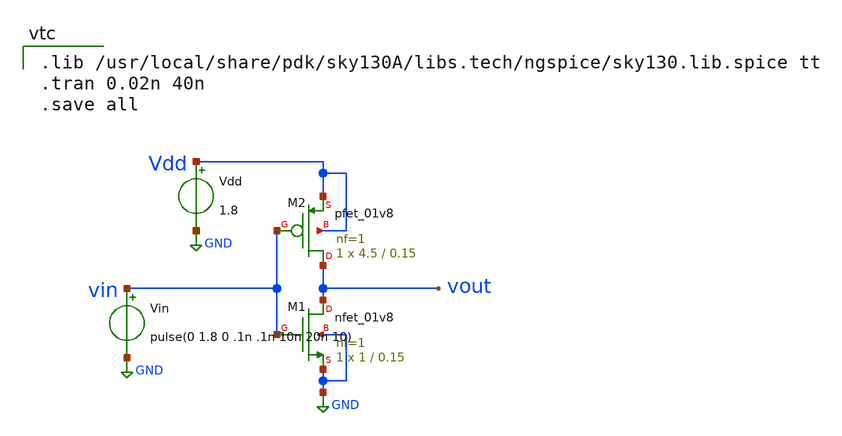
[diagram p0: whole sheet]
** sch_path: vtc_inv.sch
**.subckt vtc_inv
XM1 vout vin GND GND sky130_fd_pr__nfet_01v8 L=0.15 W=1 nf=1 ad='int((nf+1)/2) * W/nf * 0.29' as='int((nf+2)/2) * W/nf * 0.29'
+ pd='2*int((nf+1)/2) * (W/nf + 0.29)' ps='2*int((nf+2)/2) * (W/nf + 0.29)' nrd='0.29 / W' nrs='0.29 / W'
+ sa=0 sb=0 sd=0 mult=1 m=1
XM2 vout vin Vdd Vdd sky130_fd_pr__pfet_01v8 L=0.15 W=4.5 nf=1 ad='int((nf+1)/2) * W/nf * 0.29' as='int((nf+2)/2) * W/nf * 0.29'
+ pd='2*int((nf+1)/2) * (W/nf + 0.29)' ps='2*int((nf+2)/2) * (W/nf + 0.29)' nrd='0.29 / W' nrs='0.29 / W'
+ sa=0 sb=0 sd=0 mult=1 m=1
Vin vin GND pulse(0 1.8 0 .1n .1n 10n 20n 10)
Vdd Vdd GND 1.8
**** begin user architecture code

.lib /usr/local/share/pdk/sky130A/libs.tech/ngspice/sky130.lib.spice tt
.tran 0.02n 40n
.save all

**** end user architecture code
**.ends
.GLOBAL GND
.end
